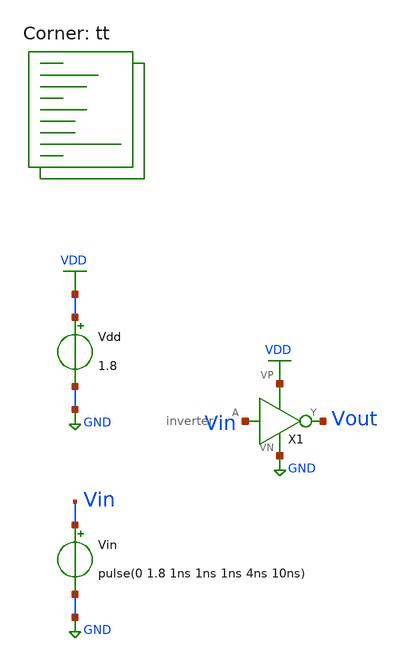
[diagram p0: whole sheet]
** sch_path: projects/inverter_tutorial/xschem_ngspice/inverter_tran.sch
**.subckt inverter_tran
Vin Vin GND pulse(0 1.8 1ns 1ns 1ns 4ns 10ns)
Vdd VDD GND 1.8
X1 Vin Vout VDD GND inverter
**** begin user architecture code



.control

  save all
  tran 0.001n 0.2u
  remzerovec
  write tb_inverter_tran.raw
  set appendwrite
  reset

.endc




.lib $::SKYWATER_MODELS/sky130.lib.spice tt
**** end user architecture code
**.ends

* expanding   symbol:
*+  /foss/designs/my_design/projects/inverter_tutorial/xschem_ngspice/inverter.sym # of pins=4
** sym_path: projects/inverter_tutorial/xschem_ngspice/inverter.sym
** sch_path: projects/inverter_tutorial/xschem_ngspice/inverter.sch
.subckt inverter A Y VP VN
*.ipin A
*.iopin VP
*.iopin VN
*.opin Y
XM1 Y A VN VN sky130_fd_pr__nfet_01v8 L=0.15 W=1 nf=1 ad='int((nf+1)/2) * W/nf * 0.29' as='int((nf+2)/2) * W/nf * 0.29'
+ pd='2*int((nf+1)/2) * (W/nf + 0.29)' ps='2*int((nf+2)/2) * (W/nf + 0.29)' nrd='0.29 / W' nrs='0.29 / W'
+ sa=0 sb=0 sd=0 mult=1 m=1
XM2 Y A VP VP sky130_fd_pr__pfet_01v8 L=0.15 W=1 nf=1 ad='int((nf+1)/2) * W/nf * 0.29' as='int((nf+2)/2) * W/nf * 0.29'
+ pd='2*int((nf+1)/2) * (W/nf + 0.29)' ps='2*int((nf+2)/2) * (W/nf + 0.29)' nrd='0.29 / W' nrs='0.29 / W'
+ sa=0 sb=0 sd=0 mult=1 m=1
.ends

.GLOBAL VDD
.GLOBAL GND
.end
